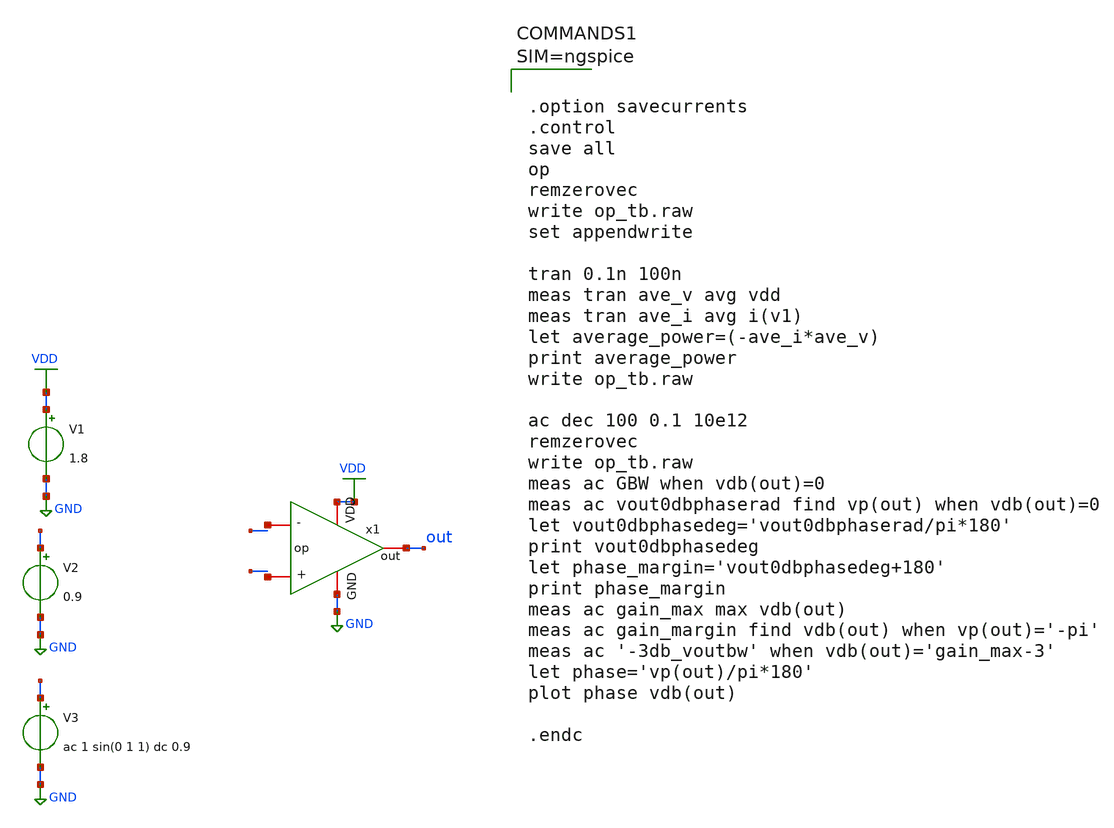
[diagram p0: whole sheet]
** sch_path: xschem/op_tb.sch
**.subckt op_tb
V1 VDD GND 1.8
V2 - GND 0.9
V3 + GND ac 1 sin(0 1 1) dc 0.9
x1 VDD out net1 net2 GND op
**** begin user architecture code

** opencircuitdesign pdks install
.lib $::SKYWATER_MODELS/sky130.lib.spice tt





.option savecurrents
.control
save all
op
remzerovec
write op_tb.raw
set appendwrite

tran 0.1n 100n
meas tran ave_v avg vdd
meas tran ave_i avg i(v1)
let average_power=(-ave_i*ave_v)
print average_power
write op_tb.raw

ac dec 100 0.1 10e12
remzerovec
write op_tb.raw
meas ac GBW when vdb(out)=0
meas ac vout0dbphaserad find vp(out) when vdb(out)=0
let vout0dbphasedeg='vout0dbphaserad/pi*180'
print vout0dbphasedeg
let phase_margin='vout0dbphasedeg+180'
print phase_margin
meas ac gain_max max vdb(out)
meas ac gain_margin find vdb(out) when vp(out)='-pi'
meas ac '-3db_voutbw' when vdb(out)='gain_max-3'
let phase='vp(out)/pi*180'
plot phase vdb(out)

.endc



**** end user architecture code
**.ends

* expanding   symbol:  op.sym # of pins=5
** sym_path: xschem/op.sym
** sch_path: xschem/op.sch
.subckt op VDD out - + GND
*.iopin VDD
*.iopin GND
*.iopin -
*.iopin +
*.iopin out
**** begin user architecture code


.param L=2.7
.param W=1.5


**** end user architecture code
XM1 net1 net2 VDD VDD sky130_fd_pr__pfet_01v8_lvt L={L} W={W} nf=1 ad='int((nf+1)/2) * W/nf * 0.29' as='int((nf+2)/2) * W/nf * 0.29'
+ pd='2*int((nf+1)/2) * (W/nf + 0.29)' ps='2*int((nf+2)/2) * (W/nf + 0.29)' nrd='0.29 / W' nrs='0.29 / W'
+ sa=0 sb=0 sd=0 mult=4 m=4
XM2 net2 net2 VDD VDD sky130_fd_pr__pfet_01v8_lvt L={L} W={W} nf=1 ad='int((nf+1)/2) * W/nf * 0.29' as='int((nf+2)/2) * W/nf * 0.29'
+ pd='2*int((nf+1)/2) * (W/nf + 0.29)' ps='2*int((nf+2)/2) * (W/nf + 0.29)' nrd='0.29 / W' nrs='0.29 / W'
+ sa=0 sb=0 sd=0 mult=4 m=4
XM3 net1 + net3 GND sky130_fd_pr__nfet_01v8_lvt L={L} W={W} nf=1 ad='int((nf+1)/2) * W/nf * 0.29' as='int((nf+2)/2) * W/nf * 0.29'
+ pd='2*int((nf+1)/2) * (W/nf + 0.29)' ps='2*int((nf+2)/2) * (W/nf + 0.29)' nrd='0.29 / W' nrs='0.29 / W'
+ sa=0 sb=0 sd=0 mult=4 m=4
XM4 net2 - net3 GND sky130_fd_pr__nfet_01v8_lvt L={L} W={W} nf=1 ad='int((nf+1)/2) * W/nf * 0.29' as='int((nf+2)/2) * W/nf * 0.29'
+ pd='2*int((nf+1)/2) * (W/nf + 0.29)' ps='2*int((nf+2)/2) * (W/nf + 0.29)' nrd='0.29 / W' nrs='0.29 / W'
+ sa=0 sb=0 sd=0 mult=4 m=4
XM5 net3 bias GND GND sky130_fd_pr__nfet_01v8_lvt L={L} W={W} nf=1 ad='int((nf+1)/2) * W/nf * 0.29' as='int((nf+2)/2) * W/nf * 0.29'
+ pd='2*int((nf+1)/2) * (W/nf + 0.29)' ps='2*int((nf+2)/2) * (W/nf + 0.29)' nrd='0.29 / W' nrs='0.29 / W'
+ sa=0 sb=0 sd=0 mult=4 m=4
XM6 bias net4 VDD VDD sky130_fd_pr__pfet_01v8_lvt L={L*2} W={W/2} nf=1 ad='int((nf+1)/2) * W/nf * 0.29'
+ as='int((nf+2)/2) * W/nf * 0.29' pd='2*int((nf+1)/2) * (W/nf + 0.29)' ps='2*int((nf+2)/2) * (W/nf + 0.29)'
+ nrd='0.29 / W' nrs='0.29 / W' sa=0 sb=0 sd=0 mult=4 m=4
XM7 net4 net4 VDD VDD sky130_fd_pr__pfet_01v8_lvt L={L*2} W={W/2} nf=1 ad='int((nf+1)/2) * W/nf * 0.29'
+ as='int((nf+2)/2) * W/nf * 0.29' pd='2*int((nf+1)/2) * (W/nf + 0.29)' ps='2*int((nf+2)/2) * (W/nf + 0.29)'
+ nrd='0.29 / W' nrs='0.29 / W' sa=0 sb=0 sd=0 mult=4 m=4
XM8 net4 bias GND GND sky130_fd_pr__nfet_01v8_lvt L={L*2} W={W/2} nf=1 ad='int((nf+1)/2) * W/nf * 0.29'
+ as='int((nf+2)/2) * W/nf * 0.29' pd='2*int((nf+1)/2) * (W/nf + 0.29)' ps='2*int((nf+2)/2) * (W/nf + 0.29)'
+ nrd='0.29 / W' nrs='0.29 / W' sa=0 sb=0 sd=0 mult=4 m=4
XM9 bias bias GND GND sky130_fd_pr__nfet_01v8_lvt L={L*2} W={W/2} nf=1 ad='int((nf+1)/2) * W/nf * 0.29'
+ as='int((nf+2)/2) * W/nf * 0.29' pd='2*int((nf+1)/2) * (W/nf + 0.29)' ps='2*int((nf+2)/2) * (W/nf + 0.29)'
+ nrd='0.29 / W' nrs='0.29 / W' sa=0 sb=0 sd=0 mult=4 m=4
XM10 out bias GND GND sky130_fd_pr__nfet_01v8_lvt L={L} W={W/2} nf=1 ad='int((nf+1)/2) * W/nf * 0.29'
+ as='int((nf+2)/2) * W/nf * 0.29' pd='2*int((nf+1)/2) * (W/nf + 0.29)' ps='2*int((nf+2)/2) * (W/nf + 0.29)'
+ nrd='0.29 / W' nrs='0.29 / W' sa=0 sb=0 sd=0 mult=4 m=4
XM11 out net1 VDD VDD sky130_fd_pr__pfet_01v8_lvt L={L} W={W} nf=1 ad='int((nf+1)/2) * W/nf * 0.29' as='int((nf+2)/2) * W/nf * 0.29'
+ pd='2*int((nf+1)/2) * (W/nf + 0.29)' ps='2*int((nf+2)/2) * (W/nf + 0.29)' nrd='0.29 / W' nrs='0.29 / W'
+ sa=0 sb=0 sd=0 mult=4 m=4
C2 out net5 1p m=1
R2 net5 net1 40k m=1
.ends

.GLOBAL VDD
.GLOBAL GND
.end
